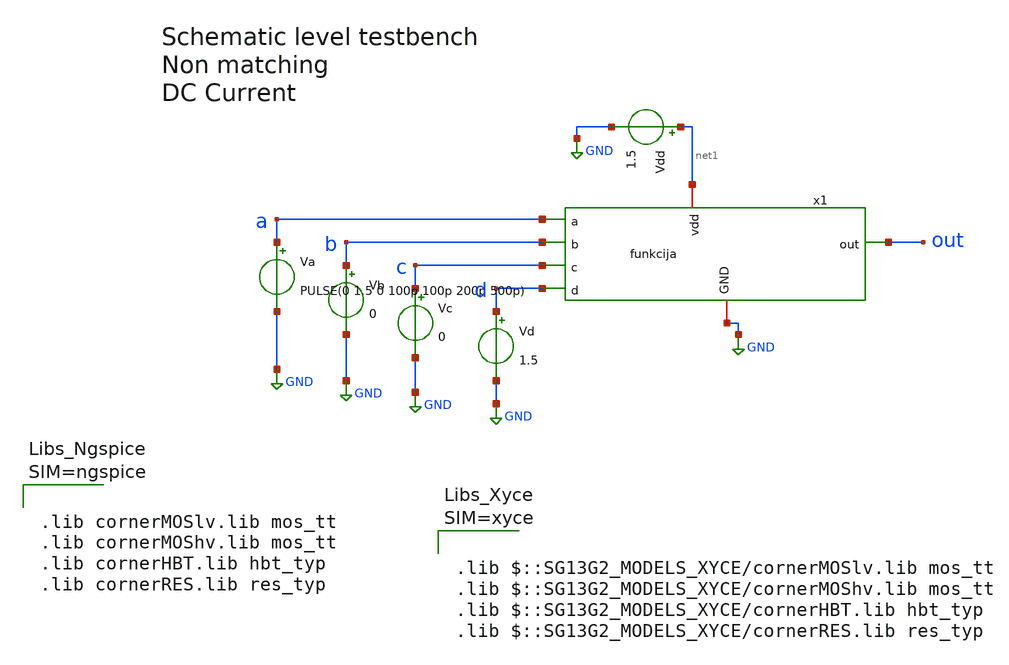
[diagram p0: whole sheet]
** sch_path: projekat/slucaj_2/testbench/tb_dc_current.sch
**.subckt tb_dc_current
Va a GND PULSE(0 1.5 0 100p 100p 200p 500p)
Vb b GND 0
Vc c GND 0
Vd d GND 1.5
Vdd net1 GND 1.5
x1 net1 out d a c b GND funkcija
**** begin user architecture code



.lib cornerMOSlv.lib mos_tt
.lib cornerMOShv.lib mos_tt
.lib cornerHBT.lib hbt_typ
.lib cornerRES.lib res_typ








* DC sweep ulaznog napona Va od 0 do 1.5V sa korakom 0.01V

.dc Va 0 1.5 0.01

.control
  run

  wrdata /home/Nikola.Jankovic/projekat/slucaj_2/python/struja.txt v(a) i(Vdd)

  plot -i(Vdd)
.endc

**** end user architecture code
**.ends

* expanding   symbol:  /home/Nikola.Jankovic/projekat/slucaj_2/schematic/funkcija.sym # of pins=7
** sym_path: projekat/slucaj_2/schematic/funkcija.sym
** sch_path: projekat/slucaj_2/schematic/funkcija.sch
.subckt funkcija vdd out d a c b GND
*.ipin a
*.ipin b
*.ipin c
*.ipin d
*.iopin vdd
*.iopin GND
*.opin out
XM1 net1 a GND GND sg13_lv_nmos w=0.3u l=0.13u ng=1 m=1 mm_ok=1
XM2 net1 b GND GND sg13_lv_nmos w=0.3u l=0.13u ng=1 m=1 mm_ok=1
XM3 net1 c GND GND sg13_lv_nmos w=0.3u l=0.13u ng=1 m=1 mm_ok=1
XM4 out d net1 GND sg13_lv_nmos w=0.3u l=0.13u ng=1 m=1 mm_ok=1
XM5 net2 a vdd vdd sg13_lv_pmos w=0.9u l=0.13u ng=1 m=1 mm_ok=1
XM6 net3 b net2 vdd sg13_lv_pmos w=0.9u l=0.13u ng=1 m=1 mm_ok=1
XM7 out c net3 vdd sg13_lv_pmos w=0.9u l=0.13u ng=1 m=1 mm_ok=1
XM8 out d vdd vdd sg13_lv_pmos w=0.3u l=0.13u ng=1 m=1 mm_ok=1
.ends

.GLOBAL GND
.end
